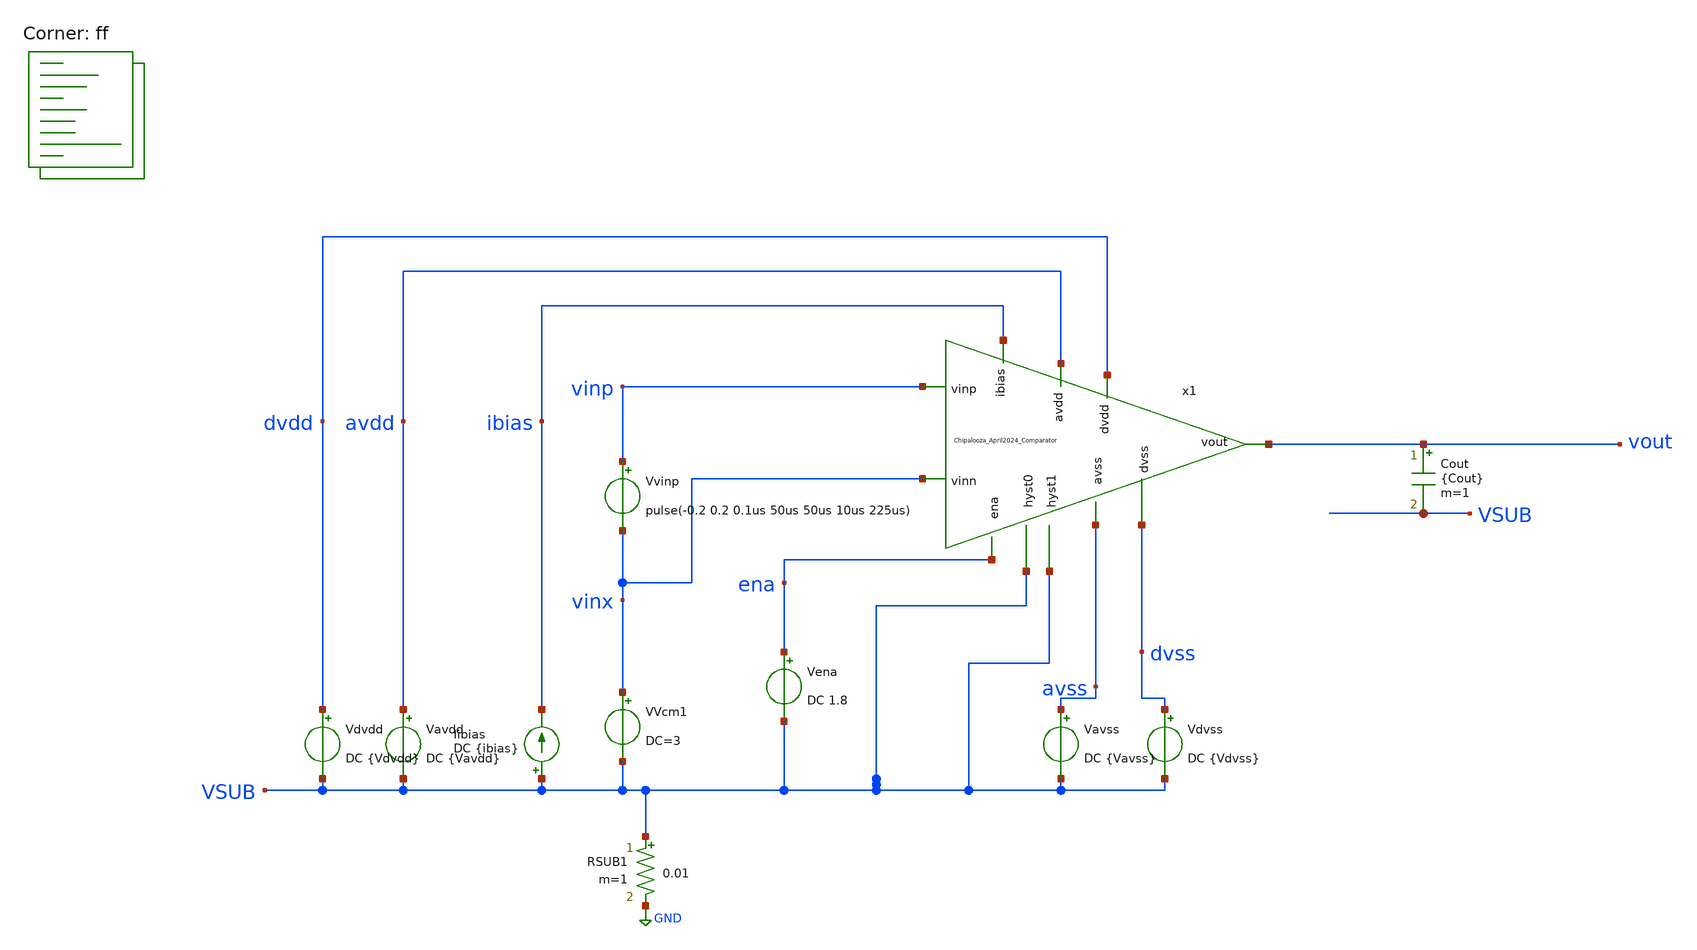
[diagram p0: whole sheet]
** sch_path: Chipalooza_April2024_Comparator/xschem/TB_hysteresis(Copy1).sch
**.subckt TB_hysteresis(Copy1)
Vavdd avdd VSUB DC {Vavdd}
Vdvdd dvdd VSUB DC {Vdvdd}
Vena ena VSUB DC 1.8
Vavss avss VSUB DC {Vavss}
Vdvss dvss VSUB DC {Vdvss}
Iibias VSUB ibias DC {ibias}
RSUB1 VSUB GND 0.01 m=1
VVcm1 vinx VSUB DC=3
Vvinp vinp vinx pulse(-0.2 0.2 0.1us 50us 50us 10us 225us)
x1 VSUB VSUB avdd vinp avss vinx dvdd dvss vout ibias ena Chipalooza_April2024_Comparator
Cout vout VSUB {Cout} m=1
**** begin user architecture code

* this option enables mos model bin
* selection based on W/NF instead of W
*.option wnflag=1
.option savecurrents
.option save all
.option temperature=80

.control

.param vavdd=3.3 cout=0 vdvdd=1.8 vavss=0
.param vdvss=0 ibias=1u

*dc VVcm 0 3.3 0.1
*plot v(vout) v(inx)

tran 0.1u 850u
*plot v(vout) v(vinp)

meas tran tr1 TRIG AT=0u TARG v(vout) VAL=1.75 RISE=1
meas tran vin_tr1 find v(vinp) at=tr1

meas tran tf1 TRIG AT=0u TARG v(vout) VAL=0.05 FALL=1
meas tran vin_tf1 find v(vinp) at=tf1

meas tran tr2 TRIG AT=0u TARG v(vout) VAL=1.75 RISE=2
meas tran vin_tr2 find v(vinp) at=tr1

meas tran tf2 TRIG AT=0u TARG v(vout) VAL=0.05 FALL=2
meas tran vin_tf2 find v(vinp) at=tf2

meas tran tr3 TRIG AT=0u TARG v(vout) VAL=1.75 RISE=3
meas tran vin_tr3 find v(vinp) at=tr3

meas tran tf3 TRIG AT=0u TARG v(vout) VAL=0.05 FALL=3
meas tran vin_tf3 find v(vinp) at=tf3

meas tran tr4 TRIG AT=0u TARG v(vout) VAL=1.75 RISE=4
meas tran vin_tr4 find v(vinp) at=tr4

meas tran tf4 TRIG AT=0u TARG v(vout) VAL=0.05 FALL=4
meas tran vin_tf4 find v(vinp) at=tf4

let hyst1=(vin_tf1-vin_tr1)
let hyst2=(vin_tf2-vin_tr2)
let hyst3=(vin_tf3-vin_tr3)
let hyst4=(vin_tf4-vin_tr4)

print hyst1
print hyst2
print hyst3
print hyst4

meas tran vinx_tr find v(vinx) at=tr1
let vio=(vinx_tr-vin_tr1)

print vio

write TB_hysteresis.raw

echo $&hyst1 $&hyst2 $&hyst3 $&vio > {simpath}/{filename}_{N}.data


*quit 0

.endc


.lib $::SKYWATER_MODELS/sky130.lib.spice ff
**** end user architecture code
**.ends

* expanding   symbol:  Chipalooza_April2024_Comparator.sym # of pins=11
** sym_path: Chipalooza_April2024_Comparator/xschem/Chipalooza_April2024_Comparator.sym
** sch_path: Chipalooza_April2024_Comparator/xschem/Chipalooza_April2024_Comparator.sch
.subckt Chipalooza_April2024_Comparator hyst0 hyst1 avdd vinp avss vinn dvdd dvss vout ibias ena
*.ipin vinp
*.ipin vinn
*.ipin hyst0
*.ipin hyst1
*.ipin avdd
*.ipin avss
*.ipin dvdd
*.ipin dvss
*.opin vout
*.ipin ena
*.ipin ibias
XM29 SumOutBar SumOut dvdd dvdd sky130_fd_pr__pfet_01v8 L=1 W=2 nf=1 ad='int((nf+1)/2) * W/nf * 0.29'
+ as='int((nf+2)/2) * W/nf * 0.29' pd='2*int((nf+1)/2) * (W/nf + 0.29)' ps='2*int((nf+2)/2) * (W/nf + 0.29)'
+ nrd='0.29 / W' nrs='0.29 / W' sa=0 sb=0 sd=0 mult=2 m=2
XM30 SumOutBar SumOut avssi dvss sky130_fd_pr__nfet_01v8 L=1 W=2 nf=1 ad='int((nf+1)/2) * W/nf * 0.29'
+ as='int((nf+2)/2) * W/nf * 0.29' pd='2*int((nf+1)/2) * (W/nf + 0.29)' ps='2*int((nf+2)/2) * (W/nf + 0.29)'
+ nrd='0.29 / W' nrs='0.29 / W' sa=0 sb=0 sd=0 mult=2 m=2
XM25 net2 ibias avssi avss sky130_fd_pr__nfet_g5v0d10v5 L=1 W=1 nf=1 ad='int((nf+1)/2) * W/nf * 0.29'
+ as='int((nf+2)/2) * W/nf * 0.29' pd='2*int((nf+1)/2) * (W/nf + 0.29)' ps='2*int((nf+2)/2) * (W/nf + 0.29)'
+ nrd='0.29 / W' nrs='0.29 / W' sa=0 sb=0 sd=0 mult=2 m=2
C1 avss 0 2p m=1
XM38 avssi ena avss avss sky130_fd_pr__nfet_g5v0d10v5 L=1 W=32 nf=1 ad='int((nf+1)/2) * W/nf * 0.29'
+ as='int((nf+2)/2) * W/nf * 0.29' pd='2*int((nf+1)/2) * (W/nf + 0.29)' ps='2*int((nf+2)/2) * (W/nf + 0.29)'
+ nrd='0.29 / W' nrs='0.29 / W' sa=0 sb=0 sd=0 mult=8 m=8
XM39 net3 ibias avssi avss sky130_fd_pr__nfet_g5v0d10v5 L=1 W=3 nf=1 ad='int((nf+1)/2) * W/nf * 0.29'
+ as='int((nf+2)/2) * W/nf * 0.29' pd='2*int((nf+1)/2) * (W/nf + 0.29)' ps='2*int((nf+2)/2) * (W/nf + 0.29)'
+ nrd='0.29 / W' nrs='0.29 / W' sa=0 sb=0 sd=0 mult=2 m=2
XM16 vout SumOutBar dvdd dvdd sky130_fd_pr__pfet_01v8 L=1 W=2 nf=1 ad='int((nf+1)/2) * W/nf * 0.29' as='int((nf+2)/2) * W/nf * 0.29'
+ pd='2*int((nf+1)/2) * (W/nf + 0.29)' ps='2*int((nf+2)/2) * (W/nf + 0.29)' nrd='0.29 / W' nrs='0.29 / W'
+ sa=0 sb=0 sd=0 mult=2 m=2
XM18 vout SumOutBar avssi dvss sky130_fd_pr__nfet_01v8 L=1 W=2 nf=1 ad='int((nf+1)/2) * W/nf * 0.29'
+ as='int((nf+2)/2) * W/nf * 0.29' pd='2*int((nf+1)/2) * (W/nf + 0.29)' ps='2*int((nf+2)/2) * (W/nf + 0.29)'
+ nrd='0.29 / W' nrs='0.29 / W' sa=0 sb=0 sd=0 mult=2 m=2
XM4 SourceBias2 SourceBias2 avdd avdd sky130_fd_pr__pfet_g5v0d10v5 L=1 W=2 nf=1 ad='int((nf+1)/2) * W/nf * 0.29'
+ as='int((nf+2)/2) * W/nf * 0.29' pd='2*int((nf+1)/2) * (W/nf + 0.29)' ps='2*int((nf+2)/2) * (W/nf + 0.29)'
+ nrd='0.29 / W' nrs='0.29 / W' sa=0 sb=0 sd=0 mult=2 m=2
XM5 N1 SourceBias2 avdd avdd sky130_fd_pr__pfet_g5v0d10v5 L=1 W=2 nf=1 ad='int((nf+1)/2) * W/nf * 0.29'
+ as='int((nf+2)/2) * W/nf * 0.29' pd='2*int((nf+1)/2) * (W/nf + 0.29)' ps='2*int((nf+2)/2) * (W/nf + 0.29)'
+ nrd='0.29 / W' nrs='0.29 / W' sa=0 sb=0 sd=0 mult=2 m=2
XM6 N2 SourceBias2 avdd avdd sky130_fd_pr__pfet_g5v0d10v5 L=1 W=2 nf=1 ad='int((nf+1)/2) * W/nf * 0.29'
+ as='int((nf+2)/2) * W/nf * 0.29' pd='2*int((nf+1)/2) * (W/nf + 0.29)' ps='2*int((nf+2)/2) * (W/nf + 0.29)'
+ nrd='0.29 / W' nrs='0.29 / W' sa=0 sb=0 sd=0 mult=2 m=2
XM7 SumOut Bias1 N2 avdd sky130_fd_pr__pfet_g5v0d10v5 L=1 W=2 nf=1 ad='int((nf+1)/2) * W/nf * 0.29' as='int((nf+2)/2) * W/nf * 0.29'
+ pd='2*int((nf+1)/2) * (W/nf + 0.29)' ps='2*int((nf+2)/2) * (W/nf + 0.29)' nrd='0.29 / W' nrs='0.29 / W'
+ sa=0 sb=0 sd=0 mult=2 m=2
XM8 Sum Bias1 N1 avdd sky130_fd_pr__pfet_g5v0d10v5 L=1 W=2 nf=1 ad='int((nf+1)/2) * W/nf * 0.29' as='int((nf+2)/2) * W/nf * 0.29'
+ pd='2*int((nf+1)/2) * (W/nf + 0.29)' ps='2*int((nf+2)/2) * (W/nf + 0.29)' nrd='0.29 / W' nrs='0.29 / W'
+ sa=0 sb=0 sd=0 mult=2 m=2
XM9 SumOut Bias2 P2 avss sky130_fd_pr__nfet_g5v0d10v5 L=1 W=2 nf=1 ad='int((nf+1)/2) * W/nf * 0.29' as='int((nf+2)/2) * W/nf * 0.29'
+ pd='2*int((nf+1)/2) * (W/nf + 0.29)' ps='2*int((nf+2)/2) * (W/nf + 0.29)' nrd='0.29 / W' nrs='0.29 / W'
+ sa=0 sb=0 sd=0 mult=2 m=2
XM10 Sum Bias2 P1 avss sky130_fd_pr__nfet_g5v0d10v5 L=1 W=2 nf=1 ad='int((nf+1)/2) * W/nf * 0.29' as='int((nf+2)/2) * W/nf * 0.29'
+ pd='2*int((nf+1)/2) * (W/nf + 0.29)' ps='2*int((nf+2)/2) * (W/nf + 0.29)' nrd='0.29 / W' nrs='0.29 / W'
+ sa=0 sb=0 sd=0 mult=2 m=2
XM11 P2 Sum avssi avss sky130_fd_pr__nfet_g5v0d10v5 L=1 W=2 nf=1 ad='int((nf+1)/2) * W/nf * 0.29' as='int((nf+2)/2) * W/nf * 0.29'
+ pd='2*int((nf+1)/2) * (W/nf + 0.29)' ps='2*int((nf+2)/2) * (W/nf + 0.29)' nrd='0.29 / W' nrs='0.29 / W'
+ sa=0 sb=0 sd=0 mult=2 m=2
XM12 P1 Sum avssi avss sky130_fd_pr__nfet_g5v0d10v5 L=1 W=2 nf=1 ad='int((nf+1)/2) * W/nf * 0.29' as='int((nf+2)/2) * W/nf * 0.29'
+ pd='2*int((nf+1)/2) * (W/nf + 0.29)' ps='2*int((nf+2)/2) * (W/nf + 0.29)' nrd='0.29 / W' nrs='0.29 / W'
+ sa=0 sb=0 sd=0 mult=2 m=2
XM2 P2 vinn psource_input avdd sky130_fd_pr__pfet_g5v0d10v5 L=1 W=4 nf=1 ad='int((nf+1)/2) * W/nf * 0.29'
+ as='int((nf+2)/2) * W/nf * 0.29' pd='2*int((nf+1)/2) * (W/nf + 0.29)' ps='2*int((nf+2)/2) * (W/nf + 0.29)'
+ nrd='0.29 / W' nrs='0.29 / W' sa=0 sb=0 sd=0 mult=2 m=2
XM3 P1 vinp psource_input avdd sky130_fd_pr__pfet_g5v0d10v5 L=1 W=4 nf=1 ad='int((nf+1)/2) * W/nf * 0.29'
+ as='int((nf+2)/2) * W/nf * 0.29' pd='2*int((nf+1)/2) * (W/nf + 0.29)' ps='2*int((nf+2)/2) * (W/nf + 0.29)'
+ nrd='0.29 / W' nrs='0.29 / W' sa=0 sb=0 sd=0 mult=2 m=2
XM14 psource_input net4 avdd avdd sky130_fd_pr__pfet_g5v0d10v5 L=1 W=12 nf=1 ad='int((nf+1)/2) * W/nf * 0.29'
+ as='int((nf+2)/2) * W/nf * 0.29' pd='2*int((nf+1)/2) * (W/nf + 0.29)' ps='2*int((nf+2)/2) * (W/nf + 0.29)'
+ nrd='0.29 / W' nrs='0.29 / W' sa=0 sb=0 sd=0 mult=4 m=4
XM15 net4 net4 avdd avdd sky130_fd_pr__pfet_g5v0d10v5 L=1 W=8 nf=1 ad='int((nf+1)/2) * W/nf * 0.29' as='int((nf+2)/2) * W/nf * 0.29'
+ pd='2*int((nf+1)/2) * (W/nf + 0.29)' ps='2*int((nf+2)/2) * (W/nf + 0.29)' nrd='0.29 / W' nrs='0.29 / W'
+ sa=0 sb=0 sd=0 mult=2 m=2
XM17 nbias_tail PBias psource_input avdd sky130_fd_pr__pfet_g5v0d10v5 L=1 W=8 nf=1 ad='int((nf+1)/2) * W/nf * 0.29'
+ as='int((nf+2)/2) * W/nf * 0.29' pd='2*int((nf+1)/2) * (W/nf + 0.29)' ps='2*int((nf+2)/2) * (W/nf + 0.29)'
+ nrd='0.29 / W' nrs='0.29 / W' sa=0 sb=0 sd=0 mult=2 m=2
XM20 N1 vinp SourceBias0 avss sky130_fd_pr__nfet_g5v0d10v5 L=4 W=16 nf=1 ad='int((nf+1)/2) * W/nf * 0.29'
+ as='int((nf+2)/2) * W/nf * 0.29' pd='2*int((nf+1)/2) * (W/nf + 0.29)' ps='2*int((nf+2)/2) * (W/nf + 0.29)'
+ nrd='0.29 / W' nrs='0.29 / W' sa=0 sb=0 sd=0 mult=2 m=2
XM21 N2 vinn SourceBias0 avss sky130_fd_pr__nfet_g5v0d10v5 L=4 W=16 nf=1 ad='int((nf+1)/2) * W/nf * 0.29'
+ as='int((nf+2)/2) * W/nf * 0.29' pd='2*int((nf+1)/2) * (W/nf + 0.29)' ps='2*int((nf+2)/2) * (W/nf + 0.29)'
+ nrd='0.29 / W' nrs='0.29 / W' sa=0 sb=0 sd=0 mult=2 m=2
XM22 SourceBias0 nbias_tail avssi avss sky130_fd_pr__nfet_g5v0d10v5 L=1 W=12 nf=1 ad='int((nf+1)/2) * W/nf * 0.29'
+ as='int((nf+2)/2) * W/nf * 0.29' pd='2*int((nf+1)/2) * (W/nf + 0.29)' ps='2*int((nf+2)/2) * (W/nf + 0.29)'
+ nrd='0.29 / W' nrs='0.29 / W' sa=0 sb=0 sd=0 mult=4 m=4
XM23 nbias_tail nbias_tail avssi avss sky130_fd_pr__nfet_g5v0d10v5 L=1 W=12 nf=1 ad='int((nf+1)/2) * W/nf * 0.29'
+ as='int((nf+2)/2) * W/nf * 0.29' pd='2*int((nf+1)/2) * (W/nf + 0.29)' ps='2*int((nf+2)/2) * (W/nf + 0.29)'
+ nrd='0.29 / W' nrs='0.29 / W' sa=0 sb=0 sd=0 mult=2 m=2
XM28 net4 hyst_bias0 SourceBias0 avss sky130_fd_pr__nfet_g5v0d10v5 L=1 W=4 nf=1 ad='int((nf+1)/2) * W/nf * 0.29'
+ as='int((nf+2)/2) * W/nf * 0.29' pd='2*int((nf+1)/2) * (W/nf + 0.29)' ps='2*int((nf+2)/2) * (W/nf + 0.29)'
+ nrd='0.29 / W' nrs='0.29 / W' sa=0 sb=0 sd=0 mult=2 m=2
XM45 SourceBias1 ibias avssi avss sky130_fd_pr__nfet_g5v0d10v5 L=1 W=3 nf=1 ad='int((nf+1)/2) * W/nf * 0.29'
+ as='int((nf+2)/2) * W/nf * 0.29' pd='2*int((nf+1)/2) * (W/nf + 0.29)' ps='2*int((nf+2)/2) * (W/nf + 0.29)'
+ nrd='0.29 / W' nrs='0.29 / W' sa=0 sb=0 sd=0 mult=2 m=2
XM46 SourceBias1 SourceBias1 avdd avdd sky130_fd_pr__pfet_g5v0d10v5 L=1 W=12 nf=1 ad='int((nf+1)/2) * W/nf * 0.29'
+ as='int((nf+2)/2) * W/nf * 0.29' pd='2*int((nf+1)/2) * (W/nf + 0.29)' ps='2*int((nf+2)/2) * (W/nf + 0.29)'
+ nrd='0.29 / W' nrs='0.29 / W' sa=0 sb=0 sd=0 mult=4 m=4
XM47 psource_input SourceBias1 avdd avdd sky130_fd_pr__pfet_g5v0d10v5 L=1 W=12 nf=1 ad='int((nf+1)/2) * W/nf * 0.29'
+ as='int((nf+2)/2) * W/nf * 0.29' pd='2*int((nf+1)/2) * (W/nf + 0.29)' ps='2*int((nf+2)/2) * (W/nf + 0.29)'
+ nrd='0.29 / W' nrs='0.29 / W' sa=0 sb=0 sd=0 mult=4 m=4
XM48 SourceBias2 ibias avssi avss sky130_fd_pr__nfet_g5v0d10v5 L=1 W=6 nf=1 ad='int((nf+1)/2) * W/nf * 0.29'
+ as='int((nf+2)/2) * W/nf * 0.29' pd='2*int((nf+1)/2) * (W/nf + 0.29)' ps='2*int((nf+2)/2) * (W/nf + 0.29)'
+ nrd='0.29 / W' nrs='0.29 / W' sa=0 sb=0 sd=0 mult=2 m=2
XM63 PBias PBias avdd avdd sky130_fd_pr__pfet_g5v0d10v5 L=5 W=3 nf=1 ad='int((nf+1)/2) * W/nf * 0.29'
+ as='int((nf+2)/2) * W/nf * 0.29' pd='2*int((nf+1)/2) * (W/nf + 0.29)' ps='2*int((nf+2)/2) * (W/nf + 0.29)'
+ nrd='0.29 / W' nrs='0.29 / W' sa=0 sb=0 sd=0 mult=1 m=1
XM62 avdd Bias4 SourceBias3 avss sky130_fd_pr__nfet_g5v0d10v5 L=1 W=4 nf=1 ad='int((nf+1)/2) * W/nf * 0.29'
+ as='int((nf+2)/2) * W/nf * 0.29' pd='2*int((nf+1)/2) * (W/nf + 0.29)' ps='2*int((nf+2)/2) * (W/nf + 0.29)'
+ nrd='0.29 / W' nrs='0.29 / W' sa=0 sb=0 sd=0 mult=2 m=2
XM64 PBias Bias4 SourceBias3 avss sky130_fd_pr__nfet_g5v0d10v5 L=1 W=4 nf=1 ad='int((nf+1)/2) * W/nf * 0.29'
+ as='int((nf+2)/2) * W/nf * 0.29' pd='2*int((nf+1)/2) * (W/nf + 0.29)' ps='2*int((nf+2)/2) * (W/nf + 0.29)'
+ nrd='0.29 / W' nrs='0.29 / W' sa=0 sb=0 sd=0 mult=2 m=2
XM65 SourceBias3 ibias avssi avss sky130_fd_pr__nfet_g5v0d10v5 L=1 W=1 nf=1 ad='int((nf+1)/2) * W/nf * 0.29'
+ as='int((nf+2)/2) * W/nf * 0.29' pd='2*int((nf+1)/2) * (W/nf + 0.29)' ps='2*int((nf+2)/2) * (W/nf + 0.29)'
+ nrd='0.29 / W' nrs='0.29 / W' sa=0 sb=0 sd=0 mult=2 m=2
XM76 Bias1 ibias avssi avss sky130_fd_pr__nfet_g5v0d10v5 L=1 W=3 nf=1 ad='int((nf+1)/2) * W/nf * 0.29'
+ as='int((nf+2)/2) * W/nf * 0.29' pd='2*int((nf+1)/2) * (W/nf + 0.29)' ps='2*int((nf+2)/2) * (W/nf + 0.29)'
+ nrd='0.29 / W' nrs='0.29 / W' sa=0 sb=0 sd=0 mult=2 m=2
XM77 SourceBias5 ibias avssi avss sky130_fd_pr__nfet_g5v0d10v5 L=1 W=3 nf=1 ad='int((nf+1)/2) * W/nf * 0.29'
+ as='int((nf+2)/2) * W/nf * 0.29' pd='2*int((nf+1)/2) * (W/nf + 0.29)' ps='2*int((nf+2)/2) * (W/nf + 0.29)'
+ nrd='0.29 / W' nrs='0.29 / W' sa=0 sb=0 sd=0 mult=2 m=2
XM78 SourceBias6 ibias avssi avss sky130_fd_pr__nfet_g5v0d10v5 L=1 W=3 nf=1 ad='int((nf+1)/2) * W/nf * 0.29'
+ as='int((nf+2)/2) * W/nf * 0.29' pd='2*int((nf+1)/2) * (W/nf + 0.29)' ps='2*int((nf+2)/2) * (W/nf + 0.29)'
+ nrd='0.29 / W' nrs='0.29 / W' sa=0 sb=0 sd=0 mult=2 m=2
XM79 SourceBias7 ibias avssi avss sky130_fd_pr__nfet_g5v0d10v5 L=1 W=3 nf=1 ad='int((nf+1)/2) * W/nf * 0.29'
+ as='int((nf+2)/2) * W/nf * 0.29' pd='2*int((nf+1)/2) * (W/nf + 0.29)' ps='2*int((nf+2)/2) * (W/nf + 0.29)'
+ nrd='0.29 / W' nrs='0.29 / W' sa=0 sb=0 sd=0 mult=2 m=2
XM81 Bias5 ibias avssi avss sky130_fd_pr__nfet_g5v0d10v5 L=1 W=3 nf=1 ad='int((nf+1)/2) * W/nf * 0.29'
+ as='int((nf+2)/2) * W/nf * 0.29' pd='2*int((nf+1)/2) * (W/nf + 0.29)' ps='2*int((nf+2)/2) * (W/nf + 0.29)'
+ nrd='0.29 / W' nrs='0.29 / W' sa=0 sb=0 sd=0 mult=2 m=2
XM82 Bias4 ibias avssi avss sky130_fd_pr__nfet_g5v0d10v5 L=1 W=3 nf=1 ad='int((nf+1)/2) * W/nf * 0.29'
+ as='int((nf+2)/2) * W/nf * 0.29' pd='2*int((nf+1)/2) * (W/nf + 0.29)' ps='2*int((nf+2)/2) * (W/nf + 0.29)'
+ nrd='0.29 / W' nrs='0.29 / W' sa=0 sb=0 sd=0 mult=2 m=2
XM83 SourceBias10 ibias avssi avss sky130_fd_pr__nfet_g5v0d10v5 L=1 W=3 nf=1 ad='int((nf+1)/2) * W/nf * 0.29'
+ as='int((nf+2)/2) * W/nf * 0.29' pd='2*int((nf+1)/2) * (W/nf + 0.29)' ps='2*int((nf+2)/2) * (W/nf + 0.29)'
+ nrd='0.29 / W' nrs='0.29 / W' sa=0 sb=0 sd=0 mult=2 m=2
XM54 M55Source M55Drain avssi avss sky130_fd_pr__nfet_g5v0d10v5 L=1.5 W=6 nf=1 ad='int((nf+1)/2) * W/nf * 0.29'
+ as='int((nf+2)/2) * W/nf * 0.29' pd='2*int((nf+1)/2) * (W/nf + 0.29)' ps='2*int((nf+2)/2) * (W/nf + 0.29)'
+ nrd='0.29 / W' nrs='0.29 / W' sa=0 sb=0 sd=0 mult=2 m=2
XM55 M55Drain Bias2 M55Source avss sky130_fd_pr__nfet_g5v0d10v5 L=1 W=9 nf=1 ad='int((nf+1)/2) * W/nf * 0.29'
+ as='int((nf+2)/2) * W/nf * 0.29' pd='2*int((nf+1)/2) * (W/nf + 0.29)' ps='2*int((nf+2)/2) * (W/nf + 0.29)'
+ nrd='0.29 / W' nrs='0.29 / W' sa=0 sb=0 sd=0 mult=2 m=2
XM56 Bias2 Bias2 avssi avss sky130_fd_pr__nfet_g5v0d10v5 L=2 W=0.5 nf=1 ad='int((nf+1)/2) * W/nf * 0.29'
+ as='int((nf+2)/2) * W/nf * 0.29' pd='2*int((nf+1)/2) * (W/nf + 0.29)' ps='2*int((nf+2)/2) * (W/nf + 0.29)'
+ nrd='0.29 / W' nrs='0.29 / W' sa=0 sb=0 sd=0 mult=1 m=1
XM51 net5 net6 avdd avdd sky130_fd_pr__pfet_g5v0d10v5 L=2 W=20 nf=1 ad='int((nf+1)/2) * W/nf * 0.29'
+ as='int((nf+2)/2) * W/nf * 0.29' pd='2*int((nf+1)/2) * (W/nf + 0.29)' ps='2*int((nf+2)/2) * (W/nf + 0.29)'
+ nrd='0.29 / W' nrs='0.29 / W' sa=0 sb=0 sd=0 mult=2 m=2
XM49 net6 net6 avdd avdd sky130_fd_pr__pfet_g5v0d10v5 L=2 W=10 nf=1 ad='int((nf+1)/2) * W/nf * 0.29'
+ as='int((nf+2)/2) * W/nf * 0.29' pd='2*int((nf+1)/2) * (W/nf + 0.29)' ps='2*int((nf+2)/2) * (W/nf + 0.29)'
+ nrd='0.29 / W' nrs='0.29 / W' sa=0 sb=0 sd=0 mult=2 m=2
XM50 SourceBias4 SourceBias4 net6 avdd sky130_fd_pr__pfet_g5v0d10v5 L=1 W=10 nf=1 ad='int((nf+1)/2) * W/nf * 0.29'
+ as='int((nf+2)/2) * W/nf * 0.29' pd='2*int((nf+1)/2) * (W/nf + 0.29)' ps='2*int((nf+2)/2) * (W/nf + 0.29)'
+ nrd='0.29 / W' nrs='0.29 / W' sa=0 sb=0 sd=0 mult=2 m=2
XM52 avssi SourceBias4 net5 avdd sky130_fd_pr__pfet_g5v0d10v5 L=1 W=1 nf=1 ad='int((nf+1)/2) * W/nf * 0.29'
+ as='int((nf+2)/2) * W/nf * 0.29' pd='2*int((nf+1)/2) * (W/nf + 0.29)' ps='2*int((nf+2)/2) * (W/nf + 0.29)'
+ nrd='0.29 / W' nrs='0.29 / W' sa=0 sb=0 sd=0 mult=2 m=2
XM53 Bias1 Bias1 net5 avdd sky130_fd_pr__pfet_g5v0d10v5 L=1 W=10 nf=1 ad='int((nf+1)/2) * W/nf * 0.29'
+ as='int((nf+2)/2) * W/nf * 0.29' pd='2*int((nf+1)/2) * (W/nf + 0.29)' ps='2*int((nf+2)/2) * (W/nf + 0.29)'
+ nrd='0.29 / W' nrs='0.29 / W' sa=0 sb=0 sd=0 mult=2 m=2
XM57 net7 net8 avdd avdd sky130_fd_pr__pfet_g5v0d10v5 L=2 W=20 nf=1 ad='int((nf+1)/2) * W/nf * 0.29'
+ as='int((nf+2)/2) * W/nf * 0.29' pd='2*int((nf+1)/2) * (W/nf + 0.29)' ps='2*int((nf+2)/2) * (W/nf + 0.29)'
+ nrd='0.29 / W' nrs='0.29 / W' sa=0 sb=0 sd=0 mult=2 m=2
XM58 net8 net8 avdd avdd sky130_fd_pr__pfet_g5v0d10v5 L=2 W=10 nf=1 ad='int((nf+1)/2) * W/nf * 0.29'
+ as='int((nf+2)/2) * W/nf * 0.29' pd='2*int((nf+1)/2) * (W/nf + 0.29)' ps='2*int((nf+2)/2) * (W/nf + 0.29)'
+ nrd='0.29 / W' nrs='0.29 / W' sa=0 sb=0 sd=0 mult=2 m=2
XM59 SourceBias10 SourceBias10 net8 avdd sky130_fd_pr__pfet_g5v0d10v5 L=1 W=10 nf=1 ad='int((nf+1)/2) * W/nf * 0.29'
+ as='int((nf+2)/2) * W/nf * 0.29' pd='2*int((nf+1)/2) * (W/nf + 0.29)' ps='2*int((nf+2)/2) * (W/nf + 0.29)'
+ nrd='0.29 / W' nrs='0.29 / W' sa=0 sb=0 sd=0 mult=2 m=2
XM60 avssi SourceBias10 net7 avdd sky130_fd_pr__pfet_g5v0d10v5 L=1 W=1 nf=1 ad='int((nf+1)/2) * W/nf * 0.29'
+ as='int((nf+2)/2) * W/nf * 0.29' pd='2*int((nf+1)/2) * (W/nf + 0.29)' ps='2*int((nf+2)/2) * (W/nf + 0.29)'
+ nrd='0.29 / W' nrs='0.29 / W' sa=0 sb=0 sd=0 mult=2 m=2
XM61 Bias4 Bias4 net7 avdd sky130_fd_pr__pfet_g5v0d10v5 L=1 W=5 nf=1 ad='int((nf+1)/2) * W/nf * 0.29'
+ as='int((nf+2)/2) * W/nf * 0.29' pd='2*int((nf+1)/2) * (W/nf + 0.29)' ps='2*int((nf+2)/2) * (W/nf + 0.29)'
+ nrd='0.29 / W' nrs='0.29 / W' sa=0 sb=0 sd=0 mult=2 m=2
XM66 net9 net10 avdd avdd sky130_fd_pr__pfet_g5v0d10v5 L=2 W=20 nf=1 ad='int((nf+1)/2) * W/nf * 0.29'
+ as='int((nf+2)/2) * W/nf * 0.29' pd='2*int((nf+1)/2) * (W/nf + 0.29)' ps='2*int((nf+2)/2) * (W/nf + 0.29)'
+ nrd='0.29 / W' nrs='0.29 / W' sa=0 sb=0 sd=0 mult=2 m=2
XM67 net10 net10 avdd avdd sky130_fd_pr__pfet_g5v0d10v5 L=2 W=20 nf=1 ad='int((nf+1)/2) * W/nf * 0.29'
+ as='int((nf+2)/2) * W/nf * 0.29' pd='2*int((nf+1)/2) * (W/nf + 0.29)' ps='2*int((nf+2)/2) * (W/nf + 0.29)'
+ nrd='0.29 / W' nrs='0.29 / W' sa=0 sb=0 sd=0 mult=2 m=2
XM68 SourceBias7 SourceBias7 net10 avdd sky130_fd_pr__pfet_g5v0d10v5 L=1 W=10 nf=1 ad='int((nf+1)/2) * W/nf * 0.29'
+ as='int((nf+2)/2) * W/nf * 0.29' pd='2*int((nf+1)/2) * (W/nf + 0.29)' ps='2*int((nf+2)/2) * (W/nf + 0.29)'
+ nrd='0.29 / W' nrs='0.29 / W' sa=0 sb=0 sd=0 mult=2 m=2
XM69 avssi SourceBias7 net9 avdd sky130_fd_pr__pfet_g5v0d10v5 L=1 W=1 nf=1 ad='int((nf+1)/2) * W/nf * 0.29'
+ as='int((nf+2)/2) * W/nf * 0.29' pd='2*int((nf+1)/2) * (W/nf + 0.29)' ps='2*int((nf+2)/2) * (W/nf + 0.29)'
+ nrd='0.29 / W' nrs='0.29 / W' sa=0 sb=0 sd=0 mult=2 m=2
XM70 Bias5 Bias5 net9 avdd sky130_fd_pr__pfet_g5v0d10v5 L=1 W=5 nf=1 ad='int((nf+1)/2) * W/nf * 0.29'
+ as='int((nf+2)/2) * W/nf * 0.29' pd='2*int((nf+1)/2) * (W/nf + 0.29)' ps='2*int((nf+2)/2) * (W/nf + 0.29)'
+ nrd='0.29 / W' nrs='0.29 / W' sa=0 sb=0 sd=0 mult=2 m=2
XM72 SourceBias5 SourceBias5 avdd avdd sky130_fd_pr__pfet_g5v0d10v5 L=1 W=12 nf=1 ad='int((nf+1)/2) * W/nf * 0.29'
+ as='int((nf+2)/2) * W/nf * 0.29' pd='2*int((nf+1)/2) * (W/nf + 0.29)' ps='2*int((nf+2)/2) * (W/nf + 0.29)'
+ nrd='0.29 / W' nrs='0.29 / W' sa=0 sb=0 sd=0 mult=4 m=4
XM73 M55Drain SourceBias5 avdd avdd sky130_fd_pr__pfet_g5v0d10v5 L=1 W=12 nf=1 ad='int((nf+1)/2) * W/nf * 0.29'
+ as='int((nf+2)/2) * W/nf * 0.29' pd='2*int((nf+1)/2) * (W/nf + 0.29)' ps='2*int((nf+2)/2) * (W/nf + 0.29)'
+ nrd='0.29 / W' nrs='0.29 / W' sa=0 sb=0 sd=0 mult=4 m=4
XM74 SourceBias6 SourceBias6 avdd avdd sky130_fd_pr__pfet_g5v0d10v5 L=1 W=12 nf=1 ad='int((nf+1)/2) * W/nf * 0.29'
+ as='int((nf+2)/2) * W/nf * 0.29' pd='2*int((nf+1)/2) * (W/nf + 0.29)' ps='2*int((nf+2)/2) * (W/nf + 0.29)'
+ nrd='0.29 / W' nrs='0.29 / W' sa=0 sb=0 sd=0 mult=4 m=4
XM75 Bias2 SourceBias6 avdd avdd sky130_fd_pr__pfet_g5v0d10v5 L=1 W=12 nf=1 ad='int((nf+1)/2) * W/nf * 0.29'
+ as='int((nf+2)/2) * W/nf * 0.29' pd='2*int((nf+1)/2) * (W/nf + 0.29)' ps='2*int((nf+2)/2) * (W/nf + 0.29)'
+ nrd='0.29 / W' nrs='0.29 / W' sa=0 sb=0 sd=0 mult=4 m=4
XM1 SourceBias0 ibias avssi avss sky130_fd_pr__nfet_g5v0d10v5 L=1 W=3 nf=1 ad='int((nf+1)/2) * W/nf * 0.29'
+ as='int((nf+2)/2) * W/nf * 0.29' pd='2*int((nf+1)/2) * (W/nf + 0.29)' ps='2*int((nf+2)/2) * (W/nf + 0.29)'
+ nrd='0.29 / W' nrs='0.29 / W' sa=0 sb=0 sd=0 mult=2 m=2
XM31 net1 hyst0 net2 avss sky130_fd_pr__nfet_01v8 L=1 W=1 nf=1 ad='int((1 + 1)/2) * 1 / 1 * 0.29' as='int((1 + 2)/2) * 1 / 1 * 0.29'
+ pd='2*int((1 + 1)/2) * (1 / 1 + 0.29)' ps='2*int((1 + 2)/2) * (1 / 1 + 0.29)' nrd='0.29 / 1 ' nrs='0.29 / 1 '
+ sa=0 sb=0 sd=0 mult=2 m=2
XM32 net1 hyst1 net3 avss sky130_fd_pr__nfet_01v8 L=1 W=3 nf=1 ad='int((1 + 1)/2) * 3 / 1 * 0.29' as='int((1 + 2)/2) * 3 / 1 * 0.29'
+ pd='2*int((1 + 1)/2) * (3 / 1 + 0.29)' ps='2*int((1 + 2)/2) * (3 / 1 + 0.29)' nrd='0.29 / 3 ' nrs='0.29 / 3 '
+ sa=0 sb=0 sd=0 mult=2 m=2
XM19 N1 SumOut net1 avss sky130_fd_pr__nfet_g5v0d10v5 L=1 W=2 nf=1 ad='int((nf+1)/2) * W/nf * 0.29' as='int((nf+2)/2) * W/nf * 0.29'
+ pd='2*int((nf+1)/2) * (W/nf + 0.29)' ps='2*int((nf+2)/2) * (W/nf + 0.29)' nrd='0.29 / W' nrs='0.29 / W'
+ sa=0 sb=0 sd=0 mult=2 m=2
XM24 N2 SumOutBar net1 avss sky130_fd_pr__nfet_g5v0d10v5 L=1 W=2 nf=1 ad='int((nf+1)/2) * W/nf * 0.29'
+ as='int((nf+2)/2) * W/nf * 0.29' pd='2*int((nf+1)/2) * (W/nf + 0.29)' ps='2*int((nf+2)/2) * (W/nf + 0.29)'
+ nrd='0.29 / W' nrs='0.29 / W' sa=0 sb=0 sd=0 mult=2 m=2
XM26 ibias ibias avssi avss sky130_fd_pr__nfet_g5v0d10v5 L=1 W=3 nf=1 ad='int((nf+1)/2) * W/nf * 0.29'
+ as='int((nf+2)/2) * W/nf * 0.29' pd='2*int((nf+1)/2) * (W/nf + 0.29)' ps='2*int((nf+2)/2) * (W/nf + 0.29)'
+ nrd='0.29 / W' nrs='0.29 / W' sa=0 sb=0 sd=0 mult=2 m=2
XM27 hyst_bias0 ibias avssi avss sky130_fd_pr__nfet_g5v0d10v5 L=1 W=3 nf=1 ad='int((nf+1)/2) * W/nf * 0.29'
+ as='int((nf+2)/2) * W/nf * 0.29' pd='2*int((nf+1)/2) * (W/nf + 0.29)' ps='2*int((nf+2)/2) * (W/nf + 0.29)'
+ nrd='0.29 / W' nrs='0.29 / W' sa=0 sb=0 sd=0 mult=2 m=2
XM33 hyst_bias0 hyst_bias0 avdd avdd sky130_fd_pr__pfet_g5v0d10v5 L=1 W=3 nf=1 ad='int((nf+1)/2) * W/nf * 0.29'
+ as='int((nf+2)/2) * W/nf * 0.29' pd='2*int((nf+1)/2) * (W/nf + 0.29)' ps='2*int((nf+2)/2) * (W/nf + 0.29)'
+ nrd='0.29 / W' nrs='0.29 / W' sa=0 sb=0 sd=0 mult=2 m=2
XM34 avss hyst_bias0 avdd avdd sky130_fd_pr__pfet_g5v0d10v5 L=1 W=3 nf=1 ad='int((nf+1)/2) * W/nf * 0.29'
+ as='int((nf+2)/2) * W/nf * 0.29' pd='2*int((nf+1)/2) * (W/nf + 0.29)' ps='2*int((nf+2)/2) * (W/nf + 0.29)'
+ nrd='0.29 / W' nrs='0.29 / W' sa=0 sb=0 sd=0 mult=2 m=2
.ends

.GLOBAL GND
.end
